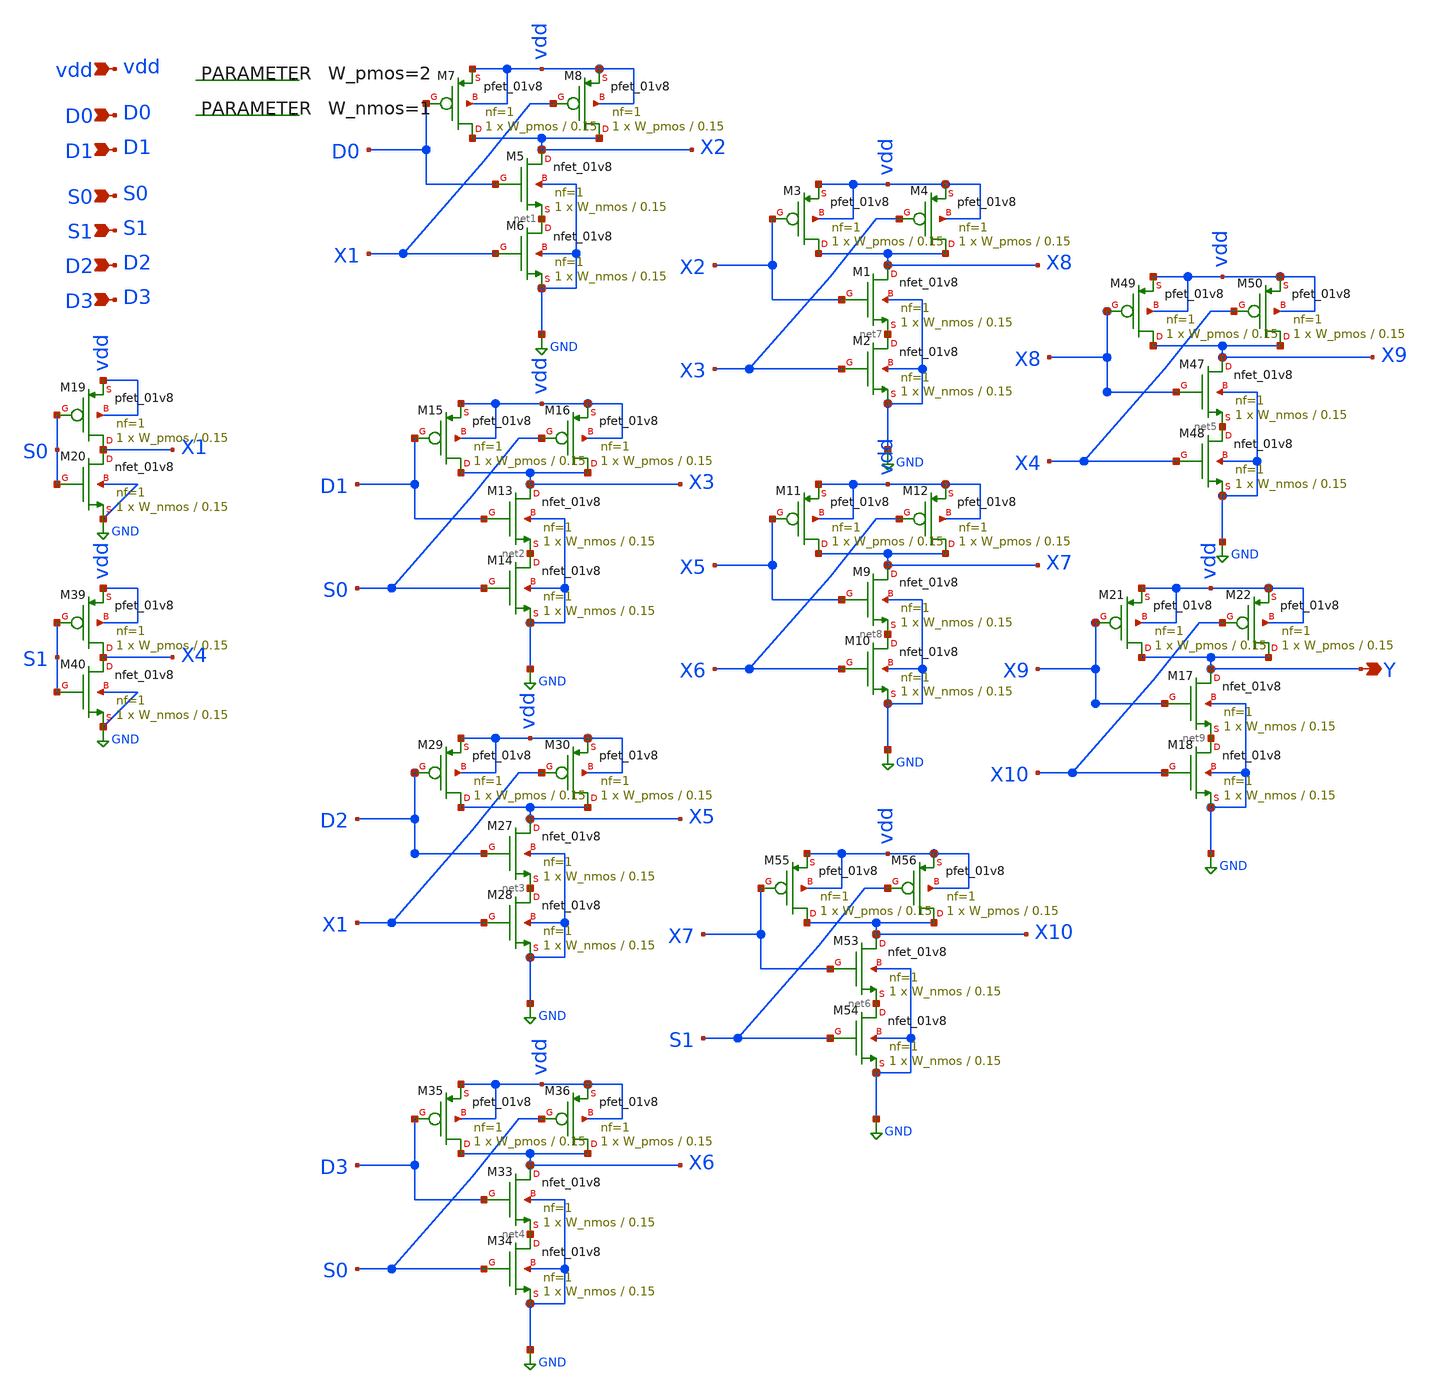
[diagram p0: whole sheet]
** sch_path: Circuit Files/circuits/circuits/4:1M_MR.sch
**.subckt 4:1M_MR D0 D1 vdd S0 D2 D3 S1 Y
*.ipin D0
*.ipin D1
*.ipin vdd
*.ipin S0
*.ipin D2
*.ipin D3
*.ipin S1
*.opin Y
XM5 X2 D0 net1 GND sky130_fd_pr__nfet_01v8 L=0.15 W=W_nmos nf=1 ad='int((nf+1)/2) * W/nf * 0.29' as='int((nf+2)/2) * W/nf * 0.29'
+ pd='2*int((nf+1)/2) * (W/nf + 0.29)' ps='2*int((nf+2)/2) * (W/nf + 0.29)' nrd='0.29 / W' nrs='0.29 / W'
+ sa=0 sb=0 sd=0 mult=1 m=1
XM6 net1 X1 GND GND sky130_fd_pr__nfet_01v8 L=0.15 W=W_nmos nf=1 ad='int((nf+1)/2) * W/nf * 0.29' as='int((nf+2)/2) * W/nf * 0.29'
+ pd='2*int((nf+1)/2) * (W/nf + 0.29)' ps='2*int((nf+2)/2) * (W/nf + 0.29)' nrd='0.29 / W' nrs='0.29 / W'
+ sa=0 sb=0 sd=0 mult=1 m=1
XM7 X2 D0 vdd vdd sky130_fd_pr__pfet_01v8 L=0.15 W=W_pmos nf=1 ad='int((nf+1)/2) * W/nf * 0.29' as='int((nf+2)/2) * W/nf * 0.29'
+ pd='2*int((nf+1)/2) * (W/nf + 0.29)' ps='2*int((nf+2)/2) * (W/nf + 0.29)' nrd='0.29 / W' nrs='0.29 / W'
+ sa=0 sb=0 sd=0 mult=1 m=1
XM8 X2 X1 vdd vdd sky130_fd_pr__pfet_01v8 L=0.15 W=W_pmos nf=1 ad='int((nf+1)/2) * W/nf * 0.29' as='int((nf+2)/2) * W/nf * 0.29'
+ pd='2*int((nf+1)/2) * (W/nf + 0.29)' ps='2*int((nf+2)/2) * (W/nf + 0.29)' nrd='0.29 / W' nrs='0.29 / W'
+ sa=0 sb=0 sd=0 mult=1 m=1
XM13 X3 D1 net2 GND sky130_fd_pr__nfet_01v8 L=0.15 W=W_nmos nf=1 ad='int((nf+1)/2) * W/nf * 0.29' as='int((nf+2)/2) * W/nf * 0.29'
+ pd='2*int((nf+1)/2) * (W/nf + 0.29)' ps='2*int((nf+2)/2) * (W/nf + 0.29)' nrd='0.29 / W' nrs='0.29 / W'
+ sa=0 sb=0 sd=0 mult=1 m=1
XM14 net2 S0 GND GND sky130_fd_pr__nfet_01v8 L=0.15 W=W_nmos nf=1 ad='int((nf+1)/2) * W/nf * 0.29' as='int((nf+2)/2) * W/nf * 0.29'
+ pd='2*int((nf+1)/2) * (W/nf + 0.29)' ps='2*int((nf+2)/2) * (W/nf + 0.29)' nrd='0.29 / W' nrs='0.29 / W'
+ sa=0 sb=0 sd=0 mult=1 m=1
XM15 X3 D1 vdd vdd sky130_fd_pr__pfet_01v8 L=0.15 W=W_pmos nf=1 ad='int((nf+1)/2) * W/nf * 0.29' as='int((nf+2)/2) * W/nf * 0.29'
+ pd='2*int((nf+1)/2) * (W/nf + 0.29)' ps='2*int((nf+2)/2) * (W/nf + 0.29)' nrd='0.29 / W' nrs='0.29 / W'
+ sa=0 sb=0 sd=0 mult=1 m=1
XM16 X3 S0 vdd vdd sky130_fd_pr__pfet_01v8 L=0.15 W=W_pmos nf=1 ad='int((nf+1)/2) * W/nf * 0.29' as='int((nf+2)/2) * W/nf * 0.29'
+ pd='2*int((nf+1)/2) * (W/nf + 0.29)' ps='2*int((nf+2)/2) * (W/nf + 0.29)' nrd='0.29 / W' nrs='0.29 / W'
+ sa=0 sb=0 sd=0 mult=1 m=1
XM19 X1 S0 vdd vdd sky130_fd_pr__pfet_01v8 L=0.15 W=W_pmos nf=1 ad='int((nf+1)/2) * W/nf * 0.29' as='int((nf+2)/2) * W/nf * 0.29'
+ pd='2*int((nf+1)/2) * (W/nf + 0.29)' ps='2*int((nf+2)/2) * (W/nf + 0.29)' nrd='0.29 / W' nrs='0.29 / W'
+ sa=0 sb=0 sd=0 mult=1 m=1
XM20 X1 S0 GND GND sky130_fd_pr__nfet_01v8 L=0.15 W=W_nmos nf=1 ad='int((nf+1)/2) * W/nf * 0.29' as='int((nf+2)/2) * W/nf * 0.29'
+ pd='2*int((nf+1)/2) * (W/nf + 0.29)' ps='2*int((nf+2)/2) * (W/nf + 0.29)' nrd='0.29 / W' nrs='0.29 / W'
+ sa=0 sb=0 sd=0 mult=1 m=1
.param W_pmos=2
.param W_nmos=1
XM27 X5 D2 net3 GND sky130_fd_pr__nfet_01v8 L=0.15 W=W_nmos nf=1 ad='int((nf+1)/2) * W/nf * 0.29' as='int((nf+2)/2) * W/nf * 0.29'
+ pd='2*int((nf+1)/2) * (W/nf + 0.29)' ps='2*int((nf+2)/2) * (W/nf + 0.29)' nrd='0.29 / W' nrs='0.29 / W'
+ sa=0 sb=0 sd=0 mult=1 m=1
XM28 net3 X1 GND GND sky130_fd_pr__nfet_01v8 L=0.15 W=W_nmos nf=1 ad='int((nf+1)/2) * W/nf * 0.29' as='int((nf+2)/2) * W/nf * 0.29'
+ pd='2*int((nf+1)/2) * (W/nf + 0.29)' ps='2*int((nf+2)/2) * (W/nf + 0.29)' nrd='0.29 / W' nrs='0.29 / W'
+ sa=0 sb=0 sd=0 mult=1 m=1
XM29 X5 D2 vdd vdd sky130_fd_pr__pfet_01v8 L=0.15 W=W_pmos nf=1 ad='int((nf+1)/2) * W/nf * 0.29' as='int((nf+2)/2) * W/nf * 0.29'
+ pd='2*int((nf+1)/2) * (W/nf + 0.29)' ps='2*int((nf+2)/2) * (W/nf + 0.29)' nrd='0.29 / W' nrs='0.29 / W'
+ sa=0 sb=0 sd=0 mult=1 m=1
XM30 X5 X1 vdd vdd sky130_fd_pr__pfet_01v8 L=0.15 W=W_pmos nf=1 ad='int((nf+1)/2) * W/nf * 0.29' as='int((nf+2)/2) * W/nf * 0.29'
+ pd='2*int((nf+1)/2) * (W/nf + 0.29)' ps='2*int((nf+2)/2) * (W/nf + 0.29)' nrd='0.29 / W' nrs='0.29 / W'
+ sa=0 sb=0 sd=0 mult=1 m=1
XM33 X6 D3 net4 GND sky130_fd_pr__nfet_01v8 L=0.15 W=W_nmos nf=1 ad='int((nf+1)/2) * W/nf * 0.29' as='int((nf+2)/2) * W/nf * 0.29'
+ pd='2*int((nf+1)/2) * (W/nf + 0.29)' ps='2*int((nf+2)/2) * (W/nf + 0.29)' nrd='0.29 / W' nrs='0.29 / W'
+ sa=0 sb=0 sd=0 mult=1 m=1
XM34 net4 S0 GND GND sky130_fd_pr__nfet_01v8 L=0.15 W=W_nmos nf=1 ad='int((nf+1)/2) * W/nf * 0.29' as='int((nf+2)/2) * W/nf * 0.29'
+ pd='2*int((nf+1)/2) * (W/nf + 0.29)' ps='2*int((nf+2)/2) * (W/nf + 0.29)' nrd='0.29 / W' nrs='0.29 / W'
+ sa=0 sb=0 sd=0 mult=1 m=1
XM35 X6 D3 vdd vdd sky130_fd_pr__pfet_01v8 L=0.15 W=W_pmos nf=1 ad='int((nf+1)/2) * W/nf * 0.29' as='int((nf+2)/2) * W/nf * 0.29'
+ pd='2*int((nf+1)/2) * (W/nf + 0.29)' ps='2*int((nf+2)/2) * (W/nf + 0.29)' nrd='0.29 / W' nrs='0.29 / W'
+ sa=0 sb=0 sd=0 mult=1 m=1
XM36 X6 S0 vdd vdd sky130_fd_pr__pfet_01v8 L=0.15 W=W_pmos nf=1 ad='int((nf+1)/2) * W/nf * 0.29' as='int((nf+2)/2) * W/nf * 0.29'
+ pd='2*int((nf+1)/2) * (W/nf + 0.29)' ps='2*int((nf+2)/2) * (W/nf + 0.29)' nrd='0.29 / W' nrs='0.29 / W'
+ sa=0 sb=0 sd=0 mult=1 m=1
XM39 X4 S1 vdd vdd sky130_fd_pr__pfet_01v8 L=0.15 W=W_pmos nf=1 ad='int((nf+1)/2) * W/nf * 0.29' as='int((nf+2)/2) * W/nf * 0.29'
+ pd='2*int((nf+1)/2) * (W/nf + 0.29)' ps='2*int((nf+2)/2) * (W/nf + 0.29)' nrd='0.29 / W' nrs='0.29 / W'
+ sa=0 sb=0 sd=0 mult=1 m=1
XM40 X4 S1 GND GND sky130_fd_pr__nfet_01v8 L=0.15 W=W_nmos nf=1 ad='int((nf+1)/2) * W/nf * 0.29' as='int((nf+2)/2) * W/nf * 0.29'
+ pd='2*int((nf+1)/2) * (W/nf + 0.29)' ps='2*int((nf+2)/2) * (W/nf + 0.29)' nrd='0.29 / W' nrs='0.29 / W'
+ sa=0 sb=0 sd=0 mult=1 m=1
XM47 X9 X8 net5 GND sky130_fd_pr__nfet_01v8 L=0.15 W=W_nmos nf=1 ad='int((nf+1)/2) * W/nf * 0.29' as='int((nf+2)/2) * W/nf * 0.29'
+ pd='2*int((nf+1)/2) * (W/nf + 0.29)' ps='2*int((nf+2)/2) * (W/nf + 0.29)' nrd='0.29 / W' nrs='0.29 / W'
+ sa=0 sb=0 sd=0 mult=1 m=1
XM48 net5 X4 GND GND sky130_fd_pr__nfet_01v8 L=0.15 W=W_nmos nf=1 ad='int((nf+1)/2) * W/nf * 0.29' as='int((nf+2)/2) * W/nf * 0.29'
+ pd='2*int((nf+1)/2) * (W/nf + 0.29)' ps='2*int((nf+2)/2) * (W/nf + 0.29)' nrd='0.29 / W' nrs='0.29 / W'
+ sa=0 sb=0 sd=0 mult=1 m=1
XM49 X9 X8 vdd vdd sky130_fd_pr__pfet_01v8 L=0.15 W=W_pmos nf=1 ad='int((nf+1)/2) * W/nf * 0.29' as='int((nf+2)/2) * W/nf * 0.29'
+ pd='2*int((nf+1)/2) * (W/nf + 0.29)' ps='2*int((nf+2)/2) * (W/nf + 0.29)' nrd='0.29 / W' nrs='0.29 / W'
+ sa=0 sb=0 sd=0 mult=1 m=1
XM50 X9 X4 vdd vdd sky130_fd_pr__pfet_01v8 L=0.15 W=W_pmos nf=1 ad='int((nf+1)/2) * W/nf * 0.29' as='int((nf+2)/2) * W/nf * 0.29'
+ pd='2*int((nf+1)/2) * (W/nf + 0.29)' ps='2*int((nf+2)/2) * (W/nf + 0.29)' nrd='0.29 / W' nrs='0.29 / W'
+ sa=0 sb=0 sd=0 mult=1 m=1
XM53 X10 X7 net6 GND sky130_fd_pr__nfet_01v8 L=0.15 W=W_nmos nf=1 ad='int((nf+1)/2) * W/nf * 0.29' as='int((nf+2)/2) * W/nf * 0.29'
+ pd='2*int((nf+1)/2) * (W/nf + 0.29)' ps='2*int((nf+2)/2) * (W/nf + 0.29)' nrd='0.29 / W' nrs='0.29 / W'
+ sa=0 sb=0 sd=0 mult=1 m=1
XM54 net6 S1 GND GND sky130_fd_pr__nfet_01v8 L=0.15 W=W_nmos nf=1 ad='int((nf+1)/2) * W/nf * 0.29' as='int((nf+2)/2) * W/nf * 0.29'
+ pd='2*int((nf+1)/2) * (W/nf + 0.29)' ps='2*int((nf+2)/2) * (W/nf + 0.29)' nrd='0.29 / W' nrs='0.29 / W'
+ sa=0 sb=0 sd=0 mult=1 m=1
XM55 X10 X7 vdd vdd sky130_fd_pr__pfet_01v8 L=0.15 W=W_pmos nf=1 ad='int((nf+1)/2) * W/nf * 0.29' as='int((nf+2)/2) * W/nf * 0.29'
+ pd='2*int((nf+1)/2) * (W/nf + 0.29)' ps='2*int((nf+2)/2) * (W/nf + 0.29)' nrd='0.29 / W' nrs='0.29 / W'
+ sa=0 sb=0 sd=0 mult=1 m=1
XM56 X10 S1 vdd vdd sky130_fd_pr__pfet_01v8 L=0.15 W=W_pmos nf=1 ad='int((nf+1)/2) * W/nf * 0.29' as='int((nf+2)/2) * W/nf * 0.29'
+ pd='2*int((nf+1)/2) * (W/nf + 0.29)' ps='2*int((nf+2)/2) * (W/nf + 0.29)' nrd='0.29 / W' nrs='0.29 / W'
+ sa=0 sb=0 sd=0 mult=1 m=1
XM1 X8 X2 net7 GND sky130_fd_pr__nfet_01v8 L=0.15 W=W_nmos nf=1 ad='int((nf+1)/2) * W/nf * 0.29' as='int((nf+2)/2) * W/nf * 0.29'
+ pd='2*int((nf+1)/2) * (W/nf + 0.29)' ps='2*int((nf+2)/2) * (W/nf + 0.29)' nrd='0.29 / W' nrs='0.29 / W'
+ sa=0 sb=0 sd=0 mult=1 m=1
XM2 net7 X3 GND GND sky130_fd_pr__nfet_01v8 L=0.15 W=W_nmos nf=1 ad='int((nf+1)/2) * W/nf * 0.29' as='int((nf+2)/2) * W/nf * 0.29'
+ pd='2*int((nf+1)/2) * (W/nf + 0.29)' ps='2*int((nf+2)/2) * (W/nf + 0.29)' nrd='0.29 / W' nrs='0.29 / W'
+ sa=0 sb=0 sd=0 mult=1 m=1
XM3 X8 X2 vdd vdd sky130_fd_pr__pfet_01v8 L=0.15 W=W_pmos nf=1 ad='int((nf+1)/2) * W/nf * 0.29' as='int((nf+2)/2) * W/nf * 0.29'
+ pd='2*int((nf+1)/2) * (W/nf + 0.29)' ps='2*int((nf+2)/2) * (W/nf + 0.29)' nrd='0.29 / W' nrs='0.29 / W'
+ sa=0 sb=0 sd=0 mult=1 m=1
XM4 X8 X3 vdd vdd sky130_fd_pr__pfet_01v8 L=0.15 W=W_pmos nf=1 ad='int((nf+1)/2) * W/nf * 0.29' as='int((nf+2)/2) * W/nf * 0.29'
+ pd='2*int((nf+1)/2) * (W/nf + 0.29)' ps='2*int((nf+2)/2) * (W/nf + 0.29)' nrd='0.29 / W' nrs='0.29 / W'
+ sa=0 sb=0 sd=0 mult=1 m=1
XM9 X7 X5 net8 GND sky130_fd_pr__nfet_01v8 L=0.15 W=W_nmos nf=1 ad='int((nf+1)/2) * W/nf * 0.29' as='int((nf+2)/2) * W/nf * 0.29'
+ pd='2*int((nf+1)/2) * (W/nf + 0.29)' ps='2*int((nf+2)/2) * (W/nf + 0.29)' nrd='0.29 / W' nrs='0.29 / W'
+ sa=0 sb=0 sd=0 mult=1 m=1
XM10 net8 X6 GND GND sky130_fd_pr__nfet_01v8 L=0.15 W=W_nmos nf=1 ad='int((nf+1)/2) * W/nf * 0.29' as='int((nf+2)/2) * W/nf * 0.29'
+ pd='2*int((nf+1)/2) * (W/nf + 0.29)' ps='2*int((nf+2)/2) * (W/nf + 0.29)' nrd='0.29 / W' nrs='0.29 / W'
+ sa=0 sb=0 sd=0 mult=1 m=1
XM11 X7 X5 vdd vdd sky130_fd_pr__pfet_01v8 L=0.15 W=W_pmos nf=1 ad='int((nf+1)/2) * W/nf * 0.29' as='int((nf+2)/2) * W/nf * 0.29'
+ pd='2*int((nf+1)/2) * (W/nf + 0.29)' ps='2*int((nf+2)/2) * (W/nf + 0.29)' nrd='0.29 / W' nrs='0.29 / W'
+ sa=0 sb=0 sd=0 mult=1 m=1
XM12 X7 X6 vdd vdd sky130_fd_pr__pfet_01v8 L=0.15 W=W_pmos nf=1 ad='int((nf+1)/2) * W/nf * 0.29' as='int((nf+2)/2) * W/nf * 0.29'
+ pd='2*int((nf+1)/2) * (W/nf + 0.29)' ps='2*int((nf+2)/2) * (W/nf + 0.29)' nrd='0.29 / W' nrs='0.29 / W'
+ sa=0 sb=0 sd=0 mult=1 m=1
XM17 Y X9 net9 GND sky130_fd_pr__nfet_01v8 L=0.15 W=W_nmos nf=1 ad='int((nf+1)/2) * W/nf * 0.29' as='int((nf+2)/2) * W/nf * 0.29'
+ pd='2*int((nf+1)/2) * (W/nf + 0.29)' ps='2*int((nf+2)/2) * (W/nf + 0.29)' nrd='0.29 / W' nrs='0.29 / W'
+ sa=0 sb=0 sd=0 mult=1 m=1
XM18 net9 X10 GND GND sky130_fd_pr__nfet_01v8 L=0.15 W=W_nmos nf=1 ad='int((nf+1)/2) * W/nf * 0.29' as='int((nf+2)/2) * W/nf * 0.29'
+ pd='2*int((nf+1)/2) * (W/nf + 0.29)' ps='2*int((nf+2)/2) * (W/nf + 0.29)' nrd='0.29 / W' nrs='0.29 / W'
+ sa=0 sb=0 sd=0 mult=1 m=1
XM21 Y X9 vdd vdd sky130_fd_pr__pfet_01v8 L=0.15 W=W_pmos nf=1 ad='int((nf+1)/2) * W/nf * 0.29' as='int((nf+2)/2) * W/nf * 0.29'
+ pd='2*int((nf+1)/2) * (W/nf + 0.29)' ps='2*int((nf+2)/2) * (W/nf + 0.29)' nrd='0.29 / W' nrs='0.29 / W'
+ sa=0 sb=0 sd=0 mult=1 m=1
XM22 Y X10 vdd vdd sky130_fd_pr__pfet_01v8 L=0.15 W=W_pmos nf=1 ad='int((nf+1)/2) * W/nf * 0.29' as='int((nf+2)/2) * W/nf * 0.29'
+ pd='2*int((nf+1)/2) * (W/nf + 0.29)' ps='2*int((nf+2)/2) * (W/nf + 0.29)' nrd='0.29 / W' nrs='0.29 / W'
+ sa=0 sb=0 sd=0 mult=1 m=1
**.ends
.GLOBAL GND
.end
